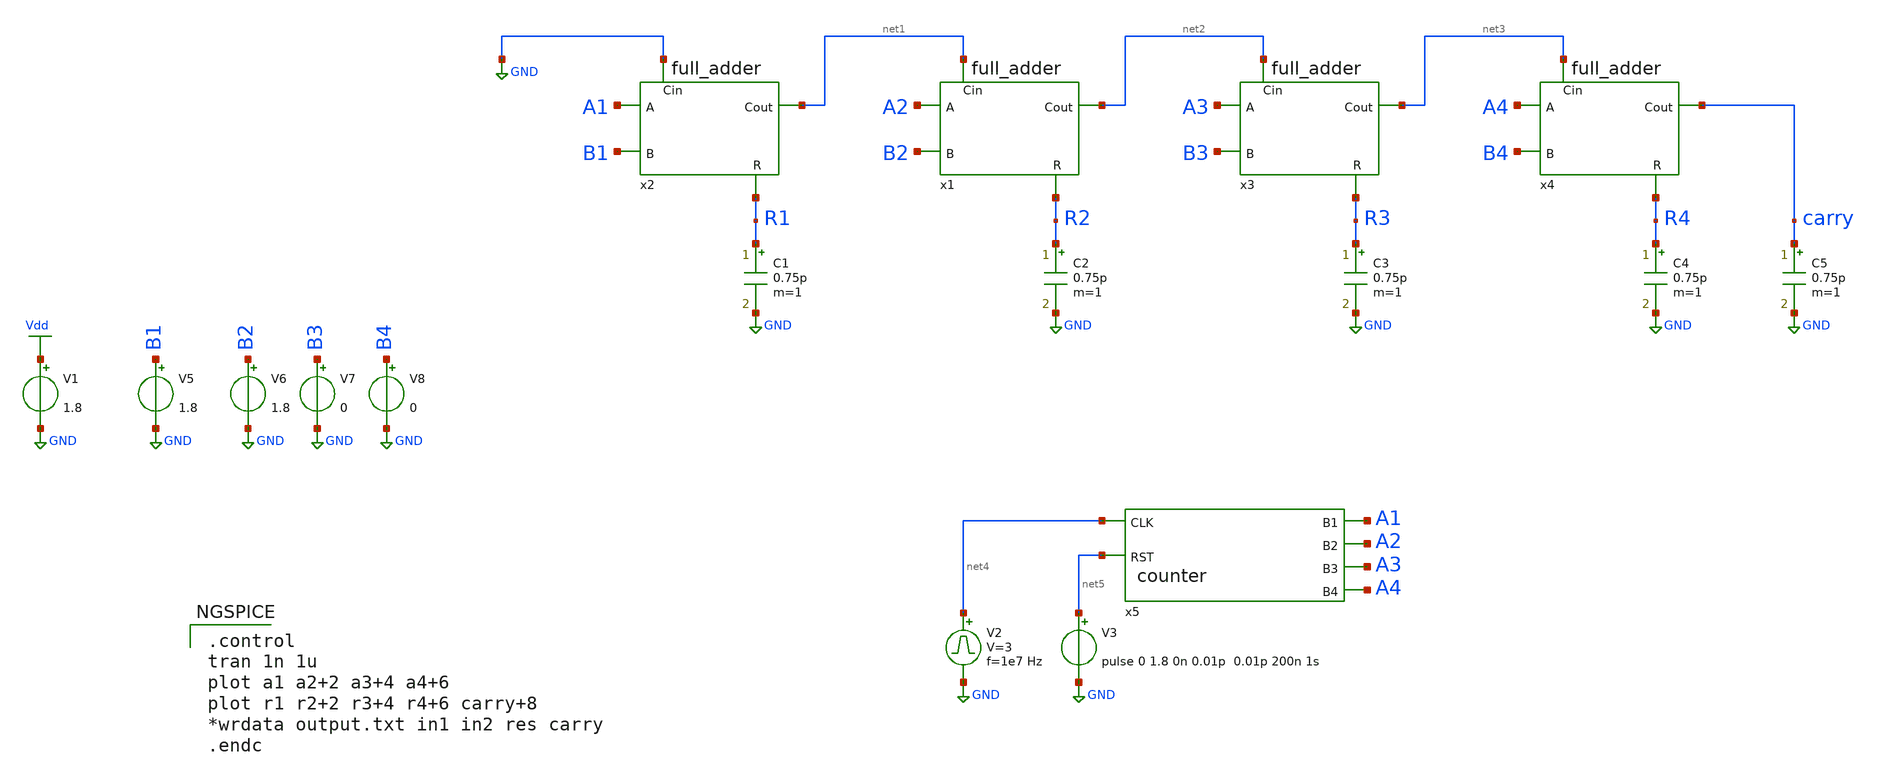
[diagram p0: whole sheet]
** sch_path: Circuiti/adder_test.sch
**.subckt adder_test
V1 Vdd GND 1.8
C1 R1 GND 0.75p m=1
x2 A1 B1 R1 GND net1 full_adder
x1 A2 B2 R2 net1 net2 full_adder
x3 A3 B3 R3 net2 net3 full_adder
x4 A4 B4 R4 net3 carry full_adder
C2 R2 GND 0.75p m=1
C3 R3 GND 0.75p m=1
C4 R4 GND 0.75p m=1
C5 carry GND 0.75p m=1
V5 B1 GND 1.8
V6 B2 GND 1.8
V7 B3 GND 0
V8 B4 GND 0
x5 A1 A2 A3 A4 net4 net5 counter
V2 net4 GND pulse 0 3 '0.495/ 1e7 ' '0.01/1e7 ' '0.01/1e7 ' '0.49/1e7 ' '1/1e7 '
V3 net5 GND pulse 0 1.8 0n 0.01p 0.01p 200n 1s
**** begin user architecture code


.lib /home/matteo/xschem_downloads/skywater-pdk/libraries/sky130_fd_pr_ngspice/latest/models/sky130.lib.spice tt

*.include /home/matteo/xschem_downloads/skywater-pdk/libraries/sky130_fd_pr_ngspice/latest/cells/nfet_01v8/sky130_fd_pr__nfet_01v8__tt.corner.spice

.param mc_mm_switch=0
.param mc_pr_switch=1



.control
tran 1n 1u
plot a1 a2+2 a3+4 a4+6
plot r1 r2+2 r3+4 r4+6 carry+8
*wrdata output.txt in1 in2 res carry
.endc


**** end user architecture code
**.ends
.GLOBAL GND
.GLOBAL Vdd
.end
